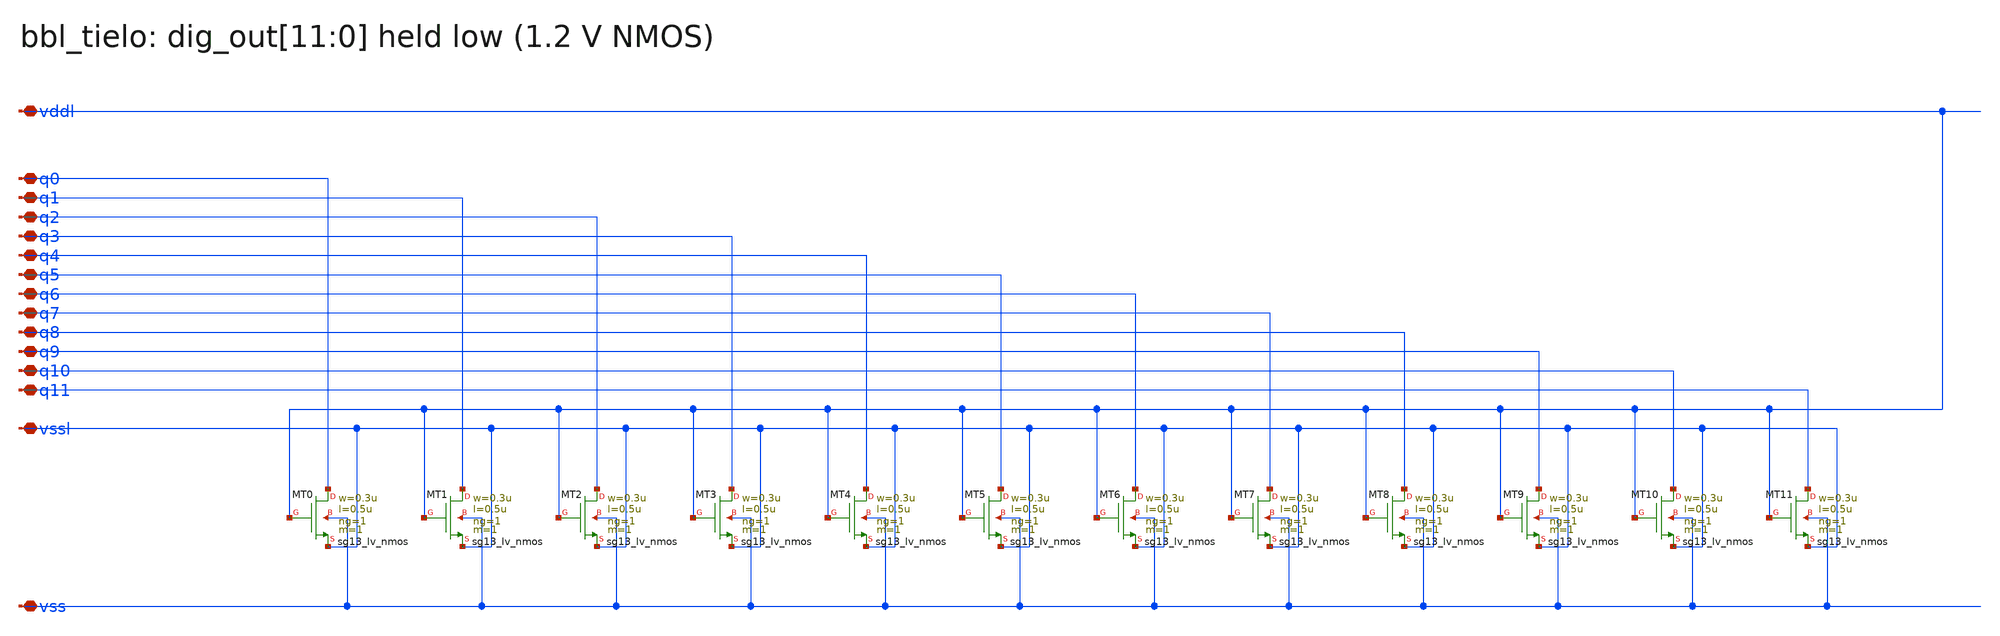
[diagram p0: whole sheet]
** sch_path: schematic/xschem/bbl_tielo.sch
**.subckt bbl_tielo vddl vssl vss q0 q1 q2 q3 q4 q5 q6 q7 q8 q9 q10 q11
*.iopin vddl
*.iopin vssl
*.iopin vss
*.iopin q0
*.iopin q1
*.iopin q2
*.iopin q3
*.iopin q4
*.iopin q5
*.iopin q6
*.iopin q7
*.iopin q8
*.iopin q9
*.iopin q10
*.iopin q11
XMT0 q0 vddl vssl vss sg13_lv_nmos w=0.3u l=0.5u ng=1 m=1 mm_ok=1
XMT1 q1 vddl vssl vss sg13_lv_nmos w=0.3u l=0.5u ng=1 m=1 mm_ok=1
XMT2 q2 vddl vssl vss sg13_lv_nmos w=0.3u l=0.5u ng=1 m=1 mm_ok=1
XMT3 q3 vddl vssl vss sg13_lv_nmos w=0.3u l=0.5u ng=1 m=1 mm_ok=1
XMT4 q4 vddl vssl vss sg13_lv_nmos w=0.3u l=0.5u ng=1 m=1 mm_ok=1
XMT5 q5 vddl vssl vss sg13_lv_nmos w=0.3u l=0.5u ng=1 m=1 mm_ok=1
XMT6 q6 vddl vssl vss sg13_lv_nmos w=0.3u l=0.5u ng=1 m=1 mm_ok=1
XMT7 q7 vddl vssl vss sg13_lv_nmos w=0.3u l=0.5u ng=1 m=1 mm_ok=1
XMT8 q8 vddl vssl vss sg13_lv_nmos w=0.3u l=0.5u ng=1 m=1 mm_ok=1
XMT9 q9 vddl vssl vss sg13_lv_nmos w=0.3u l=0.5u ng=1 m=1 mm_ok=1
XMT10 q10 vddl vssl vss sg13_lv_nmos w=0.3u l=0.5u ng=1 m=1 mm_ok=1
XMT11 q11 vddl vssl vss sg13_lv_nmos w=0.3u l=0.5u ng=1 m=1 mm_ok=1
**.ends
.end
